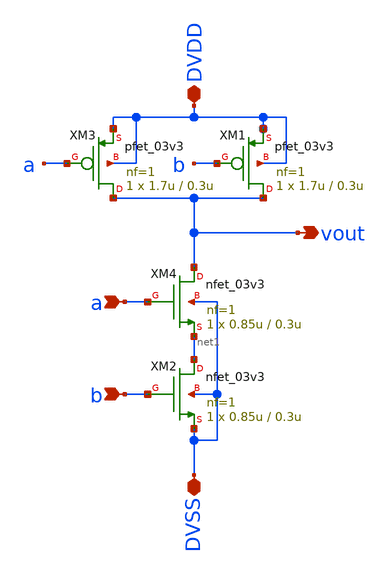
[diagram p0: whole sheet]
** sch_path: src/schematic/NAND/NAND.sch
**.subckt NAND a vout DVDD DVSS b
*.ipin a
*.opin vout
*.iopin DVDD
*.iopin DVSS
*.ipin b
XM3 vout a DVDD DVDD pfet_03v3 L=0.3u W=1.7u nf=1 ad='int((nf+1)/2) * W/nf * 0.18u' as='int((nf+2)/2) * W/nf * 0.18u'
+ pd='2*int((nf+1)/2) * (W/nf + 0.18u)' ps='2*int((nf+2)/2) * (W/nf + 0.18u)' nrd='0.18u / W' nrs='0.18u / W'
+ sa=0 sb=0 sd=0 m=1
XM4 vout a net1 DVSS nfet_03v3 L=0.3u W=0.85u nf=1 ad='int((nf+1)/2) * W/nf * 0.18u' as='int((nf+2)/2) * W/nf * 0.18u'
+ pd='2*int((nf+1)/2) * (W/nf + 0.18u)' ps='2*int((nf+2)/2) * (W/nf + 0.18u)' nrd='0.18u / W' nrs='0.18u / W'
+ sa=0 sb=0 sd=0 m=1
XM1 vout b DVDD DVDD pfet_03v3 L=0.3u W=1.7u nf=1 ad='int((nf+1)/2) * W/nf * 0.18u' as='int((nf+2)/2) * W/nf * 0.18u'
+ pd='2*int((nf+1)/2) * (W/nf + 0.18u)' ps='2*int((nf+2)/2) * (W/nf + 0.18u)' nrd='0.18u / W' nrs='0.18u / W'
+ sa=0 sb=0 sd=0 m=1
XM2 net1 b DVSS DVSS nfet_03v3 L=0.3u W=0.85u nf=1 ad='int((nf+1)/2) * W/nf * 0.18u' as='int((nf+2)/2) * W/nf * 0.18u'
+ pd='2*int((nf+1)/2) * (W/nf + 0.18u)' ps='2*int((nf+2)/2) * (W/nf + 0.18u)' nrd='0.18u / W' nrs='0.18u / W'
+ sa=0 sb=0 sd=0 m=1
**.ends
.end
